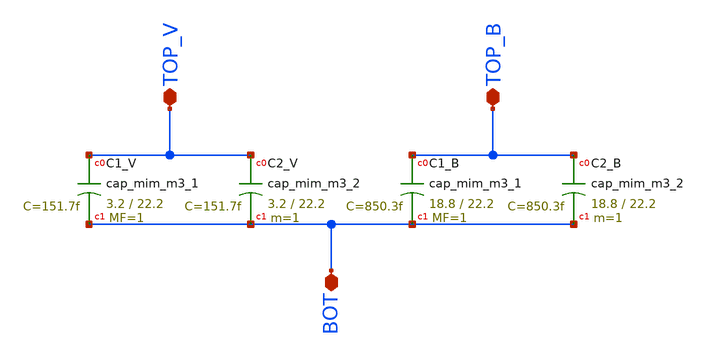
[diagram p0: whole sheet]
** sch_path: xschem/CAPOSC_v1p1.sch
**.subckt CAPOSC_v1p1 TOP_V TOP_B BOT
*.iopin TOP_V
*.iopin TOP_B
*.iopin BOT
XC1_V TOP_V BOT sky130_fd_pr__cap_mim_m3_1 W=3.2 L=22.2 MF=1 m=1
XC2_V TOP_V BOT sky130_fd_pr__cap_mim_m3_2 W=3.2 L=22.2 MF=1 m=1
XC1_B TOP_B BOT sky130_fd_pr__cap_mim_m3_1 W=18.8 L=22.2 MF=1 m=1
XC2_B TOP_B BOT sky130_fd_pr__cap_mim_m3_2 W=18.8 L=22.2 MF=1 m=1
**.ends
.end
